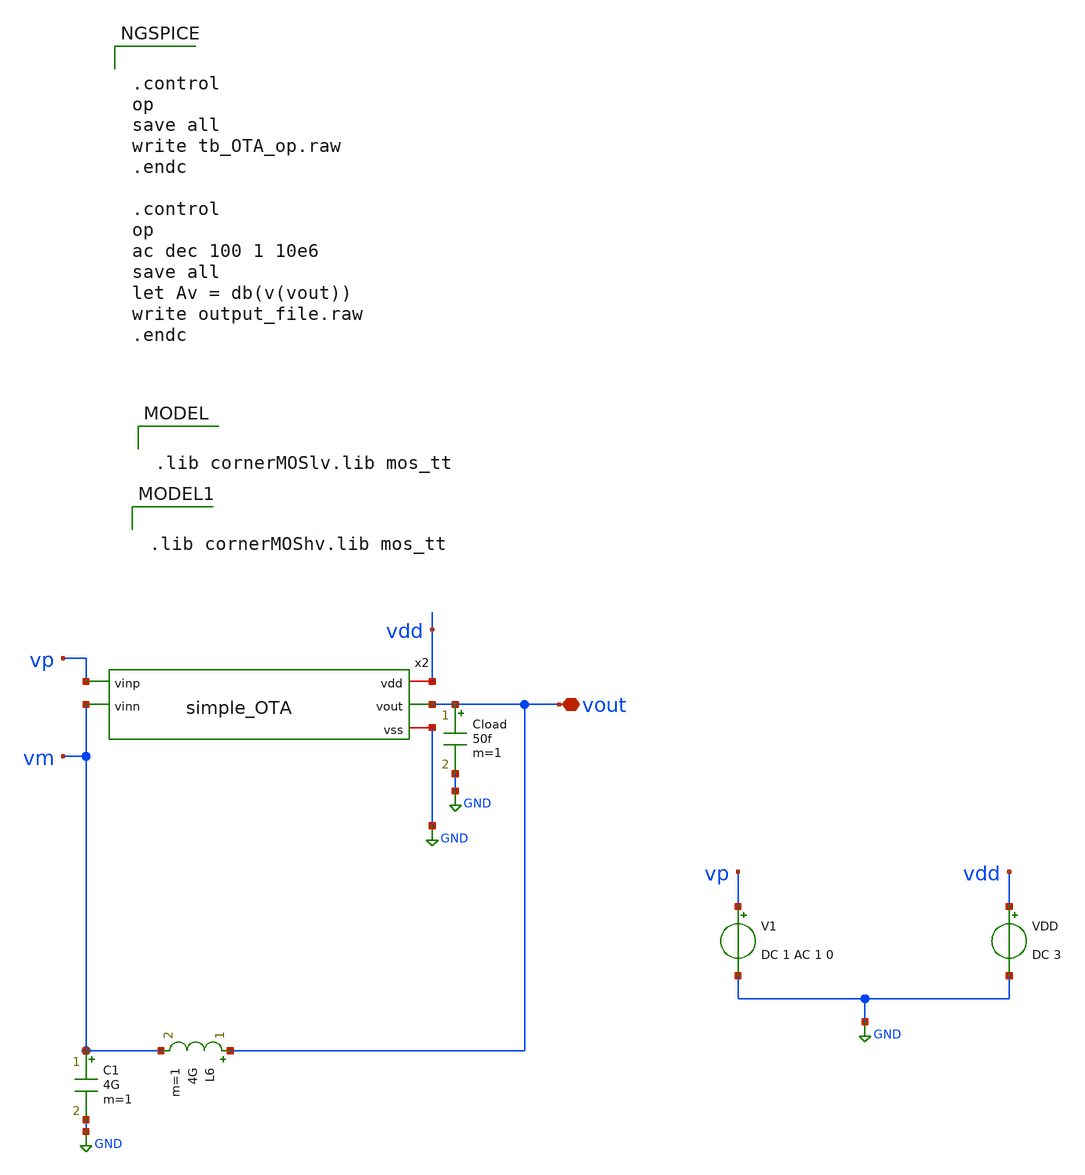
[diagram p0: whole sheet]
** sch_path: real_circuit/sandbox/OTA_tb.sch
**.subckt OTA_tb vout
*.iopin vout
V1 vp GND DC 1 AC 1 0
VDD vdd GND DC 3
Cload vout GND 50f m=1
L6 vout vm 4G m=1
C1 vm GND 4G m=1
x2 vdd vout vp vm GND simple_OTA
**** begin user architecture code

.lib cornerMOSlv.lib mos_tt



.control
op
save all
write tb_OTA_op.raw
.endc

.control
op
ac dec 100 1 10e6
save all
let Av = db(v(vout))
write output_file.raw
.endc



.lib cornerMOShv.lib mos_tt

**** end user architecture code
**.ends

* expanding   symbol:  /foss/designs/real/simple_OTA.sym # of pins=5
** sym_path: real_circuit/sandbox/simple_OTA.sym
** sch_path: real_circuit/sandbox/simple_OTA.sch
.subckt simple_OTA vdd vout vinp vinn vss
*.opin vout
*.iopin vdd
*.iopin vss
*.ipin vinp
*.ipin vinn
XM1 net1 vinp net2 vss sg13_hv_nmos w=5.75u l=4u ng=4 m=1 mm_ok=1
XM2 vout vinn net2 vss sg13_hv_nmos w=5.75u l=4u ng=4 m=1 mm_ok=1
XM3 net1 net1 vdd vdd sg13_hv_pmos w=5.16u l=4u ng=6 m=1 mm_ok=1
XM4 vout net1 vdd vdd sg13_hv_pmos w=5.16u l=4u ng=6 m=1 mm_ok=1
XM5 net2 net3 vss vss sg13_hv_nmos w=4u l=4u ng=4 m=1 mm_ok=1
XM6 net3 net3 vss vss sg13_hv_nmos w=3.9u l=4u ng=5 m=1 mm_ok=1
I0 vdd net3 6.5uA
.ends

.GLOBAL GND
.end
